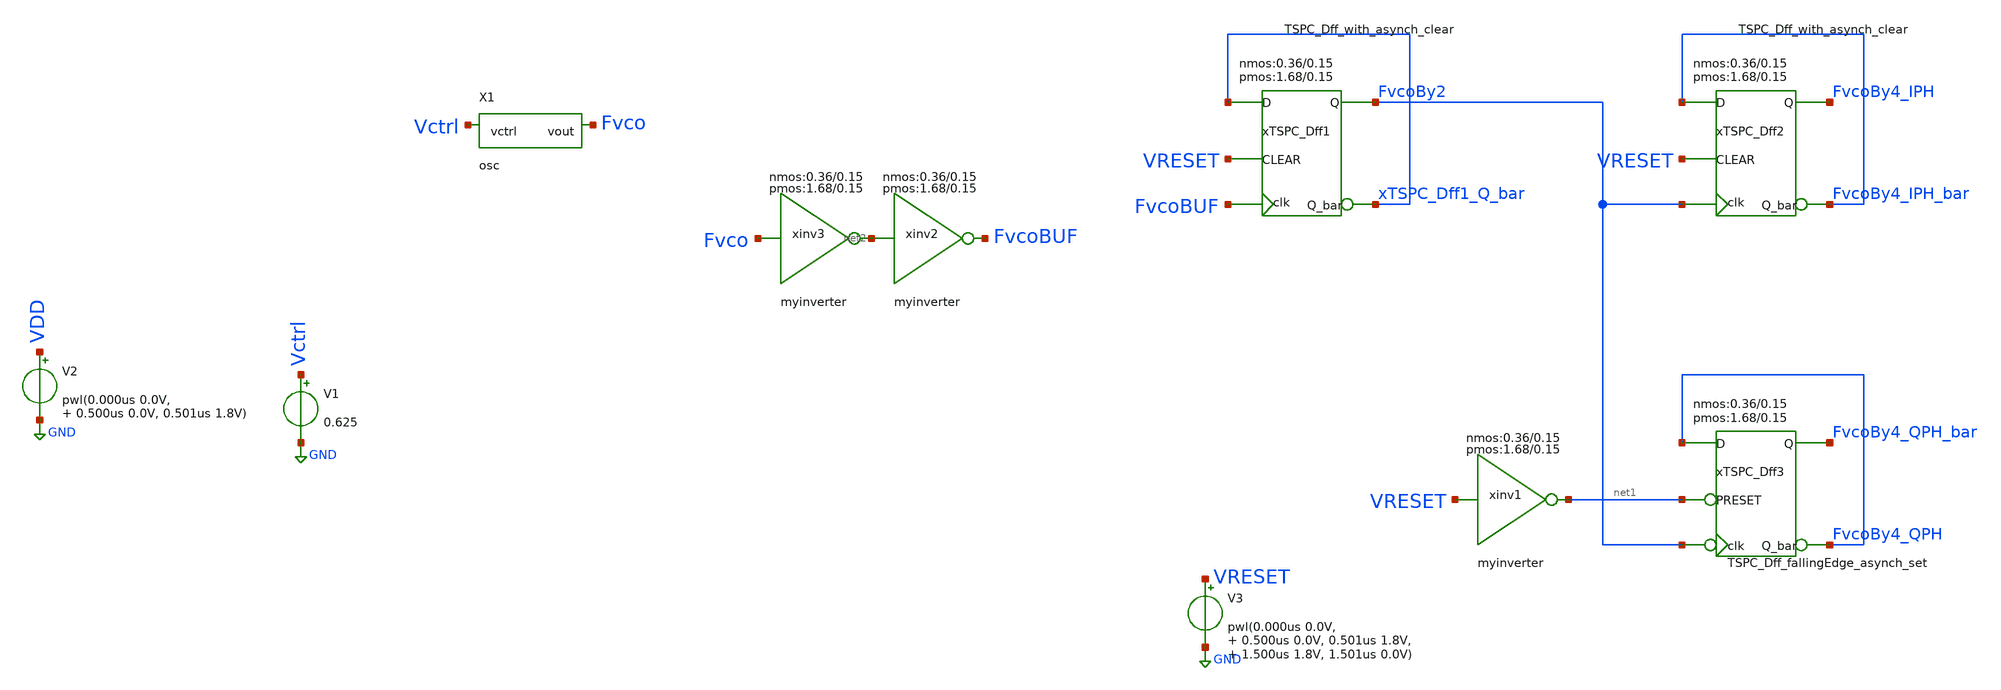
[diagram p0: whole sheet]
** sch_path: dividerOscIntegration.sch
**.subckt dividerOscIntegration
V2 VDD GND pwl(0.000us 0.0V, 0.500us 0.0V, 0.501us 1.8V)
V1 Vctrl GND 0.625
V3 VRESET GND pwl(0.000us 0.0V, 0.500us 0.0V, 0.501us 1.8V, 1.500us 1.8V, 1.501us 0.0V)
xTSPC_Dff1 FvcoBUF xTSPC_Dff1_Q_bar xTSPC_Dff1_Q_bar FvcoBy2 VRESET VDD GND
+ TSPC_Dff_with_asynch_clear wnmos=0.36 lnmos=0.15 wpmos=1.68 lpmos=0.15 m=1
xTSPC_Dff2 FvcoBy2 FvcoBy4_IPH_bar FvcoBy4_IPH_bar FvcoBy4_IPH VRESET VDD GND
+ TSPC_Dff_with_asynch_clear wnmos=0.36 lnmos=0.15 wpmos=1.68 lpmos=0.15 m=1
xTSPC_Dff3 FvcoBy2 FvcoBy4_QPH FvcoBy4_QPH FvcoBy4_QPH_bar net1 VDD GND
+ TSPC_Dff_fallingEdge_asynch_set wnmos=0.36 lnmos=0.15 wpmos=1.68 lpmos=0.15 m=1
xinv1 VRESET net1 VDD VSS myinverter wnmos=0.36 lnmos=0.15 wpmos=1.68 lpmos=0.15 m=1
xinv2 net2 FvcoBUF VDD VSS myinverter wnmos=0.36 lnmos=0.15 wpmos=1.68 lpmos=0.15 m=1
xinv3 Fvco net2 VDD VSS myinverter wnmos=0.36 lnmos=0.15 wpmos=1.68 lpmos=0.15 m=1
X1 Vctrl Fvco osc
**** begin user architecture code


.tran 0.1ns 7us
.save VRESET Fvco FvcoBy2 FvcoBy4_IPH FvcoBy4_IPH_bar FvcoBy4_QPH FvcoBy4_QPH_bar FvcoBUF


*.lib ~/open_pdks/sky130/sky130A/libs.tech/ngspice/sky130.lib.spice tt
.param mc_mm_switch=0
.param mc_pr_switch=0

.include ~/open_pdks/sky130/sky130A/libs.tech/ngspice/corners/tt/nonfet.spice


*model
.include ~/open_pdks/sky130/sky130A/libs.tech/ngspice/all.spice

*mosfet
.include ~/open_pdks/sky130/sky130A/libs.ref/sky130_fd_pr/spice/sky130_fd_pr__pfet_01v8__tt.corner.spice
.inclued ~/open_pdks/sky130/sky130A/libs.ref/sky130_fd_pr/spice/sky130_fd_pr__nfet_01v8__tt.corner.spice

*mismatch parameters
.include ~/open_pdks/sky130/sky130A/libs.ref/sky130_fd_pr/spice/sky130_fd_pr__pfet_01v8__mismatch.corner.spice
.include ~/open_pdks/sky130/sky130A/libs.ref/sky130_fd_pr/spice/sky130_fd_pr__nfet_01v8__mismatch.corner.spice

**** end user architecture code
**.ends
.GLOBAL GND
.end
